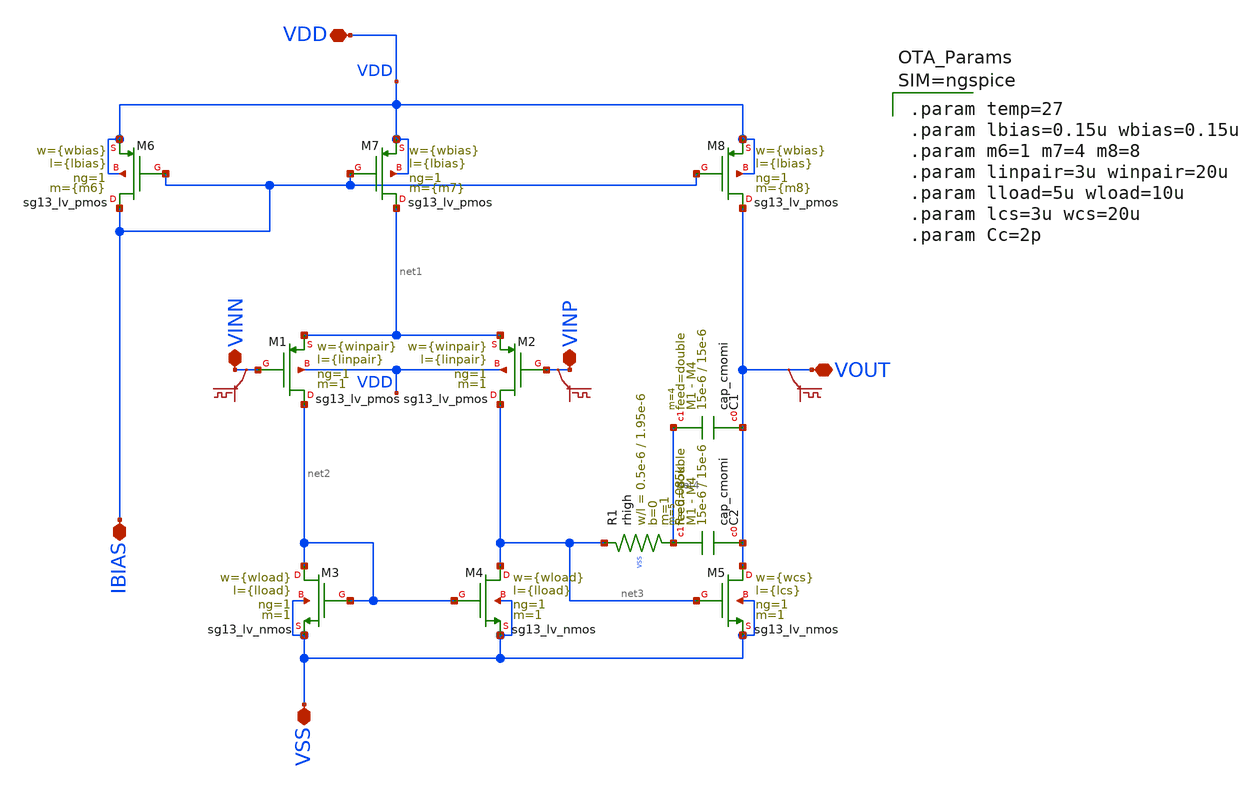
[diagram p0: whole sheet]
** sch_path: xschem/output_buffer/ota_cmos5l.sch
**.subckt ota_cmos5l IBIAS VDD VSS VOUT VINP VINN
*.iopin IBIAS
*.iopin VDD
*.iopin VSS
*.iopin VOUT
*.iopin VINP
*.iopin VINN
XM6 IBIAS IBIAS VDD VDD sg13_lv_pmos w={wbias} l={lbias} ng=1 m={m6} mm_ok=1
XM7 net1 IBIAS VDD VDD sg13_lv_pmos w={wbias} l={lbias} ng=1 m={m7} mm_ok=1
XM8 VOUT IBIAS VDD VDD sg13_lv_pmos w={wbias} l={lbias} ng=1 m={m8} mm_ok=1
XM1 net2 VINN net1 VDD sg13_lv_pmos w={winpair} l={linpair} ng=1 m=1 mm_ok=1
XM2 net3 VINP net1 VDD sg13_lv_pmos w={winpair} l={linpair} ng=1 m=1 mm_ok=1
XM3 net2 net2 VSS VSS sg13_lv_nmos w={wload} l={lload} ng=1 m=1 mm_ok=1
XM4 net3 net2 VSS VSS sg13_lv_nmos w={wload} l={lload} ng=1 m=1 mm_ok=1
XM5 VOUT net3 VSS VSS sg13_lv_nmos w={wcs} l={lcs} ng=1 m=1 mm_ok=1
XR1 net3 net4 VSS rhigh w=0.5e-6 l=1.95e-6 m=1 b=0 mm_ok=1
.save v(vinp)
.save v(vinn)
.save v(vout)
XC2 VOUT net4 cap_cmomi w=15e-6 l=15e-6 mmin=1 mmax=4 feed=double subblock=0 m=5 mm_ok=1
XC1 VOUT net4 cap_cmomi w=15e-6 l=15e-6 mmin=1 mmax=4 feed=double subblock=0 m=4 mm_ok=1
**** begin user architecture code


.param temp=27
.param lbias=0.15u wbias=0.15u
.param m6=1 m7=4 m8=8
.param linpair=3u winpair=20u
.param lload=5u wload=10u
.param lcs=3u wcs=20u
.param Cc=2p



**** end user architecture code
**.ends
.end
